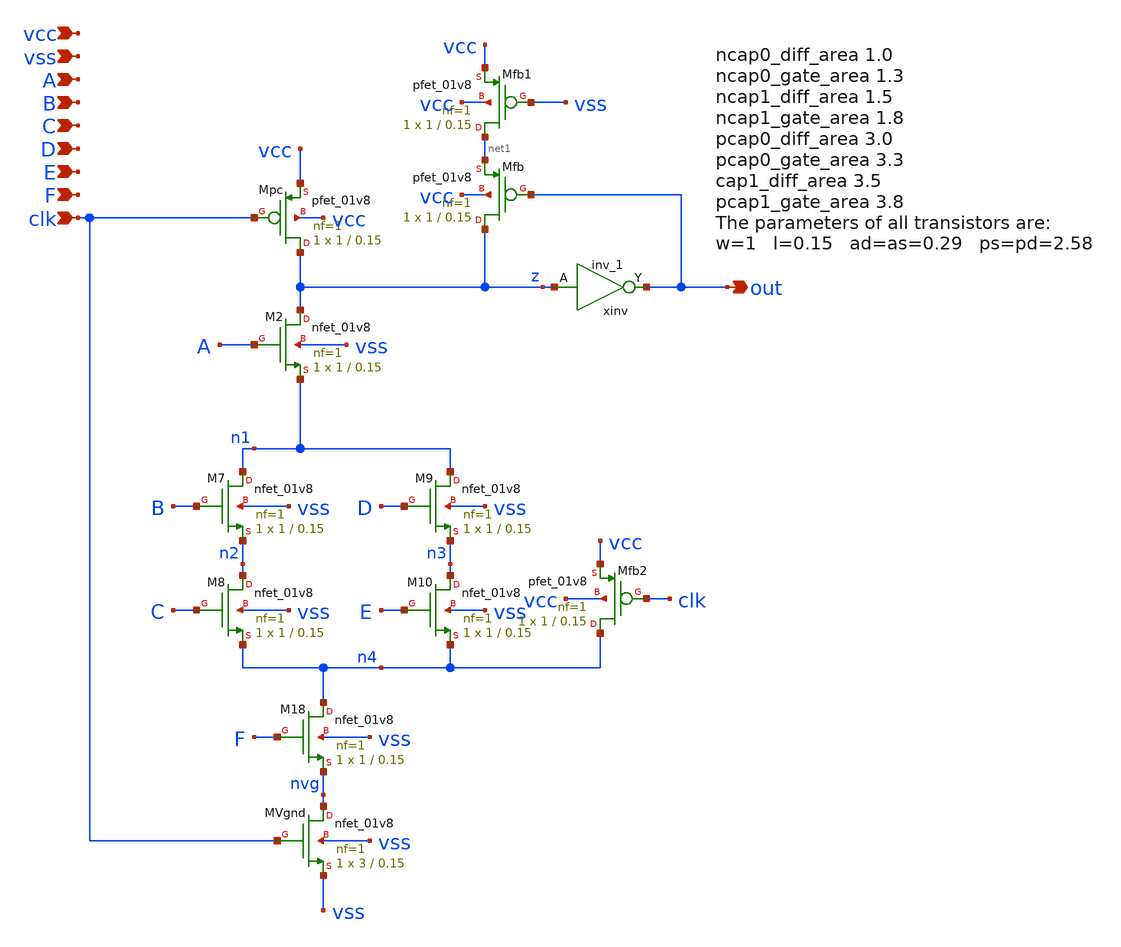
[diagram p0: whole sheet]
** sch_path: src/xe/test_cases/yxt_charge_sharing.sch
**.subckt yxt_charge_sharing clk out D C B A F E vss vcc
*.ipin clk
*.opin out
*.ipin D
*.ipin C
*.ipin B
*.ipin A
*.ipin F
*.ipin E
*.ipin vss
*.ipin vcc
XMpc z clk vcc vcc sky130_fd_pr__pfet_01v8 L=0.15 W=1 nf=1 ad='int((nf+1)/2) * W/nf * 0.29' as='int((nf+2)/2) * W/nf * 0.29'
+ pd='2*int((nf+1)/2) * (W/nf + 0.29)' ps='2*int((nf+2)/2) * (W/nf + 0.29)' nrd='0.29 / W' nrs='0.29 / W'
+ sa=0 sb=0 sd=0 mult=1 m=1
XM2 z A n1 vss sky130_fd_pr__nfet_01v8 L=0.15 W=1 nf=1 ad='int((nf+1)/2) * W/nf * 0.29' as='int((nf+2)/2) * W/nf * 0.29'
+ pd='2*int((nf+1)/2) * (W/nf + 0.29)' ps='2*int((nf+2)/2) * (W/nf + 0.29)' nrd='0.29 / W' nrs='0.29 / W'
+ sa=0 sb=0 sd=0 mult=1 m=1
xinv z vss vss vcc vcc out sky130_fd_sc_hd__inv_1
XM7 n1 B n2 vss sky130_fd_pr__nfet_01v8 L=0.15 W=1 nf=1 ad='int((nf+1)/2) * W/nf * 0.29' as='int((nf+2)/2) * W/nf * 0.29'
+ pd='2*int((nf+1)/2) * (W/nf + 0.29)' ps='2*int((nf+2)/2) * (W/nf + 0.29)' nrd='0.29 / W' nrs='0.29 / W'
+ sa=0 sb=0 sd=0 mult=1 m=1
XM8 n2 C n4 vss sky130_fd_pr__nfet_01v8 L=0.15 W=1 nf=1 ad='int((nf+1)/2) * W/nf * 0.29' as='int((nf+2)/2) * W/nf * 0.29'
+ pd='2*int((nf+1)/2) * (W/nf + 0.29)' ps='2*int((nf+2)/2) * (W/nf + 0.29)' nrd='0.29 / W' nrs='0.29 / W'
+ sa=0 sb=0 sd=0 mult=1 m=1
XM9 n1 D n3 vss sky130_fd_pr__nfet_01v8 L=0.15 W=1 nf=1 ad='int((nf+1)/2) * W/nf * 0.29' as='int((nf+2)/2) * W/nf * 0.29'
+ pd='2*int((nf+1)/2) * (W/nf + 0.29)' ps='2*int((nf+2)/2) * (W/nf + 0.29)' nrd='0.29 / W' nrs='0.29 / W'
+ sa=0 sb=0 sd=0 mult=1 m=1
XM10 n3 E n4 vss sky130_fd_pr__nfet_01v8 L=0.15 W=1 nf=1 ad='int((nf+1)/2) * W/nf * 0.29' as='int((nf+2)/2) * W/nf * 0.29'
+ pd='2*int((nf+1)/2) * (W/nf + 0.29)' ps='2*int((nf+2)/2) * (W/nf + 0.29)' nrd='0.29 / W' nrs='0.29 / W'
+ sa=0 sb=0 sd=0 mult=1 m=1
XMVgnd nvg clk vss vss sky130_fd_pr__nfet_01v8 L=0.15 W=3 nf=1 ad='int((nf+1)/2) * W/nf * 0.29' as='int((nf+2)/2) * W/nf * 0.29'
+ pd='2*int((nf+1)/2) * (W/nf + 0.29)' ps='2*int((nf+2)/2) * (W/nf + 0.29)' nrd='0.29 / W' nrs='0.29 / W'
+ sa=0 sb=0 sd=0 mult=1 m=1
XM18 n4 F nvg vss sky130_fd_pr__nfet_01v8 L=0.15 W=1 nf=1 ad='int((nf+1)/2) * W/nf * 0.29' as='int((nf+2)/2) * W/nf * 0.29'
+ pd='2*int((nf+1)/2) * (W/nf + 0.29)' ps='2*int((nf+2)/2) * (W/nf + 0.29)' nrd='0.29 / W' nrs='0.29 / W'
+ sa=0 sb=0 sd=0 mult=1 m=1
XMfb z out net1 vcc sky130_fd_pr__pfet_01v8 L=0.15 W=1 nf=1 ad='int((nf+1)/2) * W/nf * 0.29' as='int((nf+2)/2) * W/nf * 0.29'
+ pd='2*int((nf+1)/2) * (W/nf + 0.29)' ps='2*int((nf+2)/2) * (W/nf + 0.29)' nrd='0.29 / W' nrs='0.29 / W'
+ sa=0 sb=0 sd=0 mult=1 m=1
XMfb1 net1 vss vcc vcc sky130_fd_pr__pfet_01v8 L=0.15 W=1 nf=1 ad='int((nf+1)/2) * W/nf * 0.29' as='int((nf+2)/2) * W/nf * 0.29'
+ pd='2*int((nf+1)/2) * (W/nf + 0.29)' ps='2*int((nf+2)/2) * (W/nf + 0.29)' nrd='0.29 / W' nrs='0.29 / W'
+ sa=0 sb=0 sd=0 mult=1 m=1
XMfb2 n4 clk vcc vcc sky130_fd_pr__pfet_01v8 L=0.15 W=1 nf=1 ad='int((nf+1)/2) * W/nf * 0.29' as='int((nf+2)/2) * W/nf * 0.29'
+ pd='2*int((nf+1)/2) * (W/nf + 0.29)' ps='2*int((nf+2)/2) * (W/nf + 0.29)' nrd='0.29 / W' nrs='0.29 / W'
+ sa=0 sb=0 sd=0 mult=1 m=1
**** begin user architecture code

** opencircuitdesign pdks install

.subckt sky130_fd_sc_hd__inv_1 A VGND VNB VPB VPWR Y
X0 VGND A Y VNB sky130_fd_pr__nfet_01v8 w=650000u l=150000u
X1 VPWR A Y VPB sky130_fd_pr__pfet_01v8_hvt w=1e+06u l=150000u
.ends


**** end user architecture code
**.ends
.end
